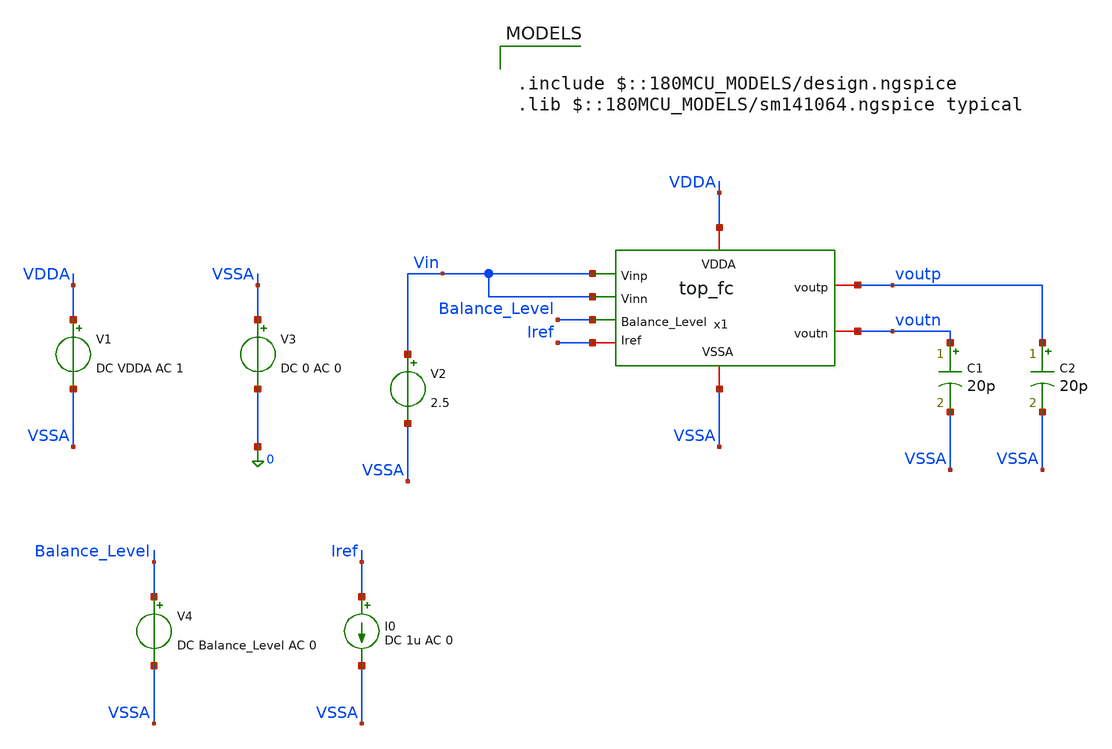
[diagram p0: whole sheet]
** sch_path: Folded_cascode/testbenches/top_fc_psrrp_tb.sch
**.subckt top_fc_psrrp_tb
x1 Balance_Level Vin voutp VDDA voutn Vin Iref VSSA top_fc
V2 Vin VSSA 2.5
C1 voutn VSSA 20p m=1
C2 voutp VSSA 20p m=1
V1 VDDA VSSA DC VDDA AC 1
V3 VSSA 0 DC 0 AC 0
V4 Balance_Level VSSA DC Balance_Level AC 0
I0 Iref VSSA DC 1u AC 0
**** begin user architecture code

.include $::180MCU_MODELS/design.ngspice
.lib $::180MCU_MODELS/sm141064.ngspice typical



.temp 27
.param VDDA = 5
.param Balance_Level = 1.5

.control
option sparse
set filetype=ascii
set wr_singlescale
set wr_vecnames
save all
save @m.x1.x1.xm1.m0[id]
save @m.x1.x1.xm1.m0[gm]
save @m.x1.x1.xm1.m0[vgs]
save @m.x1.x1.xm1.m0[vds]
save @m.x1.x1.xm1.m0[vth]
save @m.x1.x1.xm1.m0[gds]
save @m.x1.x1.xm1.m0[vdsat]

save @m.x1.x1.xm2.m0[id]
save @m.x1.x1.xm2.m0[gm]
save @m.x1.x1.xm2.m0[vgs]
save @m.x1.x1.xm2.m0[vds]
save @m.x1.x1.xm2.m0[vth]
save @m.x1.x1.xm2.m0[gds]
save @m.x1.x1.xm2.m0[vdsat]

save @m.x1.x1.xm9.m0[id]
save @m.x1.x1.xm9.m0[gm]
save @m.x1.x1.xm9.m0[vgs]
save @m.x1.x1.xm9.m0[vds]
save @m.x1.x1.xm9.m0[vth]
save @m.x1.x1.xm9.m0[gds]
save @m.x1.x1.xm9.m0[vdsat]

save @m.x1.x1.xm8.m0[id]
save @m.x1.x1.xm8.m0[gm]
save @m.x1.x1.xm8.m0[vgs]
save @m.x1.x1.xm8.m0[vds]
save @m.x1.x1.xm8.m0[vth]
save @m.x1.x1.xm8.m0[gds]
save @m.x1.x1.xm8.m0[vdsat]

save @m.x1.x1.xm6.m0[id]
save @m.x1.x1.xm6.m0[gm]
save @m.x1.x1.xm6.m0[vgs]
save @m.x1.x1.xm6.m0[vds]
save @m.x1.x1.xm6.m0[vth]
save @m.x1.x1.xm6.m0[gds]
save @m.x1.x1.xm6.m0[vdsat]

save @m.x1.x1.xm5.m0[id]
save @m.x1.x1.xm5.m0[gm]
save @m.x1.x1.xm5.m0[vgs]
save @m.x1.x1.xm5.m0[vds]
save @m.x1.x1.xm5.m0[vth]
save @m.x1.x1.xm5.m0[gds]
save @m.x1.x1.xm5.m0[vdsat]

save @m.x1.x2.xm1.m0[id]
save @m.x1.x2.xm1.m0[gm]
save @m.x1.x2.xm1.m0[vgs]
save @m.x1.x2.xm1.m0[vds]
save @m.x1.x2.xm1.m0[vth]
save @m.x1.x2.xm1.m0[gds]

save @m.x1.x2.xm2.m0[id]
save @m.x1.x2.xm2.m0[gm]
save @m.x1.x2.xm2.m0[vgs]
save @m.x1.x2.xm2.m0[vds]
save @m.x1.x2.xm2.m0[vth]
save @m.x1.x2.xm2.m0[gds]

save @m.x1.x2.xm3.m0[id]
save @m.x1.x2.xm3.m0[gm]
save @m.x1.x2.xm3.m0[vgs]
save @m.x1.x2.xm3.m0[vds]
save @m.x1.x2.xm3.m0[vth]
save @m.x1.x2.xm3.m0[gds]

save @m.x1.x2.xm4.m0[id]
save @m.x1.x2.xm4.m0[gm]
save @m.x1.x2.xm4.m0[vgs]
save @m.x1.x2.xm4.m0[vds]
save @m.x1.x2.xm4.m0[vth]
save @m.x1.x2.xm4.m0[gds]

save @m.x1.x2.xm5.m0[id]
save @m.x1.x2.xm5.m0[gm]
save @m.x1.x2.xm5.m0[vgs]
save @m.x1.x2.xm5.m0[vds]
save @m.x1.x2.xm5.m0[vth]
save @m.x1.x2.xm5.m0[gds]

save @m.x1.x2.xm6.m0[id]
save @m.x1.x2.xm6.m0[gm]
save @m.x1.x2.xm6.m0[vgs]
save @m.x1.x2.xm6.m0[vds]
save @m.x1.x2.xm6.m0[vth]
save @m.x1.x2.xm6.m0[gds]

save @m.x1.x2.xm7.m0[id]
save @m.x1.x2.xm7.m0[gm]
save @m.x1.x2.xm7.m0[vgs]
save @m.x1.x2.xm7.m0[vds]
save @m.x1.x2.xm7.m0[vth]
save @m.x1.x2.xm7.m0[gds]

save @m.x1.x2.xm8.m0[id]
save @m.x1.x2.xm8.m0[gm]
save @m.x1.x2.xm8.m0[vgs]
save @m.x1.x2.xm8.m0[vds]
save @m.x1.x2.xm8.m0[vth]
save @m.x1.x2.xm8.m0[gds]

save @m.x1.x2.xm9.m0[id]
save @m.x1.x2.xm9.m0[gm]
save @m.x1.x2.xm9.m0[vgs]
save @m.x1.x2.xm9.m0[vds]
save @m.x1.x2.xm9.m0[vth]
save @m.x1.x2.xm9.m0[gds]

save @m.x1.x3.xm1.m0[id]
save @m.x1.x3.xm1.m0[gm]
save @m.x1.x3.xm1.m0[vgs]
save @m.x1.x3.xm1.m0[vds]
save @m.x1.x3.xm1.m0[vth]
save @m.x1.x3.xm1.m0[gds]

save @m.x1.x3.xm2.m0[id]
save @m.x1.x3.xm2.m0[gm]
save @m.x1.x3.xm2.m0[vgs]
save @m.x1.x3.xm2.m0[vds]
save @m.x1.x3.xm2.m0[vth]
save @m.x1.x3.xm2.m0[gds]

save @m.x1.x3.xm3.m0[id]
save @m.x1.x3.xm3.m0[gm]
save @m.x1.x3.xm3.m0[vgs]
save @m.x1.x3.xm3.m0[vds]
save @m.x1.x3.xm3.m0[vth]
save @m.x1.x3.xm3.m0[gds]

save @m.x1.x3.xm4.m0[id]
save @m.x1.x3.xm4.m0[gm]
save @m.x1.x3.xm4.m0[vgs]
save @m.x1.x3.xm4.m0[vds]
save @m.x1.x3.xm4.m0[vth]
save @m.x1.x3.xm4.m0[gds]

save @m.x1.x3.xm5.m0[id]
save @m.x1.x3.xm5.m0[gm]
save @m.x1.x3.xm5.m0[vgs]
save @m.x1.x3.xm5.m0[vds]
save @m.x1.x3.xm5.m0[vth]
save @m.x1.x3.xm5.m0[gds]

save @m.x1.x3.xm6.m0[id]
save @m.x1.x3.xm6.m0[gm]
save @m.x1.x3.xm6.m0[vgs]
save @m.x1.x3.xm6.m0[vds]
save @m.x1.x3.xm6.m0[vth]
save @m.x1.x3.xm6.m0[gds]

save @m.x1.x3.xm7.m0[id]
save @m.x1.x3.xm7.m0[gm]
save @m.x1.x3.xm7.m0[vgs]
save @m.x1.x3.xm7.m0[vds]
save @m.x1.x3.xm7.m0[vth]
save @m.x1.x3.xm7.m0[gds]

save @m.x1.x3.xm8.m0[id]
save @m.x1.x3.xm8.m0[gm]
save @m.x1.x3.xm8.m0[vgs]
save @m.x1.x3.xm8.m0[vds]
save @m.x1.x3.xm8.m0[vth]
save @m.x1.x3.xm8.m0[gds]

save @m.x1.x3.xm9.m0[id]
save @m.x1.x3.xm9.m0[gm]
save @m.x1.x3.xm9.m0[vgs]
save @m.x1.x3.xm9.m0[vds]
save @m.x1.x3.xm9.m0[vth]
save @m.x1.x3.xm9.m0[gds]

save @m.x1.x3.xm10.m0[id]
save @m.x1.x3.xm10.m0[gm]
save @m.x1.x3.xm10.m0[vgs]
save @m.x1.x3.xm10.m0[vds]
save @m.x1.x3.xm10.m0[vth]
save @m.x1.x3.xm10.m0[gds]

save @m.x1.x3.xm11.m0[id]
save @m.x1.x3.xm11.m0[gm]
save @m.x1.x3.xm11.m0[vgs]
save @m.x1.x3.xm11.m0[vds]
save @m.x1.x3.xm11.m0[vth]
save @m.x1.x3.xm11.m0[gds]

save @m.x1.x3.xm12.m0[id]
save @m.x1.x3.xm12.m0[gm]
save @m.x1.x3.xm12.m0[vgs]
save @m.x1.x3.xm12.m0[vds]
save @m.x1.x3.xm12.m0[vth]
save @m.x1.x3.xm12.m0[gds]

save @m.x1.x3.xm13.m0[id]
save @m.x1.x3.xm13.m0[gm]
save @m.x1.x3.xm13.m0[vgs]
save @m.x1.x3.xm13.m0[vds]
save @m.x1.x3.xm13.m0[vth]
save @m.x1.x3.xm13.m0[gds]

save @m.x1.x3.xm14.m0[id]
save @m.x1.x3.xm14.m0[gm]
save @m.x1.x3.xm14.m0[vgs]
save @m.x1.x3.xm14.m0[vds]
save @m.x1.x3.xm14.m0[vth]
save @m.x1.x3.xm14.m0[gds]

save @m.x1.x3.xm15.m0[id]
save @m.x1.x3.xm15.m0[gm]
save @m.x1.x3.xm15.m0[vgs]
save @m.x1.x3.xm15.m0[vds]
save @m.x1.x3.xm15.m0[vth]
save @m.x1.x3.xm15.m0[gds]

save @m.x1.x3.xm16.m0[id]
save @m.x1.x3.xm16.m0[gm]
save @m.x1.x3.xm16.m0[vgs]
save @m.x1.x3.xm16.m0[vds]
save @m.x1.x3.xm16.m0[vth]
save @m.x1.x3.xm16.m0[gds]

save @m.x1.x3.xm17.m0[id]
save @m.x1.x3.xm17.m0[gm]
save @m.x1.x3.xm17.m0[vgs]
save @m.x1.x3.xm17.m0[vds]
save @m.x1.x3.xm17.m0[vth]
save @m.x1.x3.xm17.m0[gds]

save @m.x1.x3.xm18.m0[id]
save @m.x1.x3.xm18.m0[gm]
save @m.x1.x3.xm18.m0[vgs]
save @m.x1.x3.xm18.m0[vds]
save @m.x1.x3.xm18.m0[vth]
save @m.x1.x3.xm18.m0[gds]

save @m.x1.x3.xm21.m0[id]
save @m.x1.x3.xm21.m0[gm]
save @m.x1.x3.xm21.m0[vgs]
save @m.x1.x3.xm21.m0[vds]
save @m.x1.x3.xm21.m0[vth]
save @m.x1.x3.xm21.m0[gds]

save @m.x1.x3.xm22.m0[id]
save @m.x1.x3.xm22.m0[gm]
save @m.x1.x3.xm22.m0[vgs]
save @m.x1.x3.xm22.m0[vds]
save @m.x1.x3.xm22.m0[vth]
save @m.x1.x3.xm22.m0[gds]

op
write top_fc_op_tb.raw all

set appendwrite

ac dec 100 1 1G

* ------------------------------------------------------------
* Output components
* ------------------------------------------------------------

let vod  = v(voutp)-v(voutn)
let vocm = (v(voutp)+v(voutn))/2

* ------------------------------------------------------------
* Supply-to-output transfer functions
* ------------------------------------------------------------

let aps_p    = v(voutp)/v(VDDA)
let aps_n    = v(voutn)/v(VDDA)
let aps_diff = vod/v(VDDA)
let aps_cm   = vocm/v(VDDA)

* ------------------------------------------------------------
* Magnitude in dB
* ------------------------------------------------------------

let aps_p_db    = db(aps_p)
let aps_n_db    = db(aps_n)
let aps_diff_db = db(aps_diff)
let aps_cm_db   = db(aps_cm)

* ------------------------------------------------------------
* Output-referred supply rejection
* ------------------------------------------------------------

let psrr_diff = -aps_diff_db
let supply_rejection_cm = -aps_cm_db

* ============================================================
* Measurements: differential supply coupling
* ============================================================

meas ac aps_diff_1Hz   FIND aps_diff_db AT=1
meas ac aps_diff_1k    FIND aps_diff_db AT=1k
meas ac aps_diff_10k   FIND aps_diff_db AT=10k
meas ac aps_diff_100k  FIND aps_diff_db AT=100k
meas ac aps_diff_1Meg  FIND aps_diff_db AT=1Meg
meas ac aps_diff_10Meg FIND aps_diff_db AT=10Meg

* ============================================================
* Measurements: common-mode supply coupling
* ============================================================

meas ac aps_cm_1Hz   FIND aps_cm_db AT=1
meas ac aps_cm_1k    FIND aps_cm_db AT=1k
meas ac aps_cm_10k   FIND aps_cm_db AT=10k
meas ac aps_cm_100k  FIND aps_cm_db AT=100k
meas ac aps_cm_1Meg  FIND aps_cm_db AT=1Meg
meas ac aps_cm_10Meg FIND aps_cm_db AT=10Meg

* ============================================================
* Measurements: nominal differential supply rejection
* ============================================================

meas ac psrr_diff_1Hz   FIND psrr_diff AT=1
meas ac psrr_diff_1k    FIND psrr_diff AT=1k
meas ac psrr_diff_10k   FIND psrr_diff AT=10k
meas ac psrr_diff_100k  FIND psrr_diff AT=100k
meas ac psrr_diff_1Meg  FIND psrr_diff AT=1Meg
meas ac psrr_diff_10Meg FIND psrr_diff AT=10Meg

* ============================================================
* Measurements: common-mode supply rejection
* ============================================================

meas ac sr_cm_1Hz   FIND supply_rejection_cm AT=1
meas ac sr_cm_1k    FIND supply_rejection_cm AT=1k
meas ac sr_cm_10k   FIND supply_rejection_cm AT=10k
meas ac sr_cm_100k  FIND supply_rejection_cm AT=100k
meas ac sr_cm_1Meg  FIND supply_rejection_cm AT=1Meg
meas ac sr_cm_10Meg FIND supply_rejection_cm AT=10Meg

* ============================================================
* Print results
* ============================================================

print aps_diff_1Hz
print aps_diff_1k
print aps_diff_10k
print aps_diff_100k
print aps_diff_1Meg
print aps_diff_10Meg

print aps_cm_1Hz
print aps_cm_1k
print aps_cm_10k
print aps_cm_100k
print aps_cm_1Meg
print aps_cm_10Meg

print psrr_diff_1Hz
print psrr_diff_1k
print psrr_diff_10k
print psrr_diff_100k
print psrr_diff_1Meg
print psrr_diff_10Meg

print sr_cm_1Hz
print sr_cm_1k
print sr_cm_10k
print sr_cm_100k
print sr_cm_1Meg
print sr_cm_10Meg

* ============================================================
* Save results
* ============================================================

write top_fc_psrrp_tb.raw

* ============================================================
* Plots
* ============================================================

* Positive and negative output responses to VDDA disturbance
plot aps_p_db aps_n_db

* Differential supply coupling
plot aps_diff_db

* Common-mode supply coupling
plot aps_cm_db

* Nominal differential supply rejection
plot psrr_diff

* Common-mode supply rejection
plot supply_rejection_cm
.endc


**** end user architecture code
**.ends
.end
